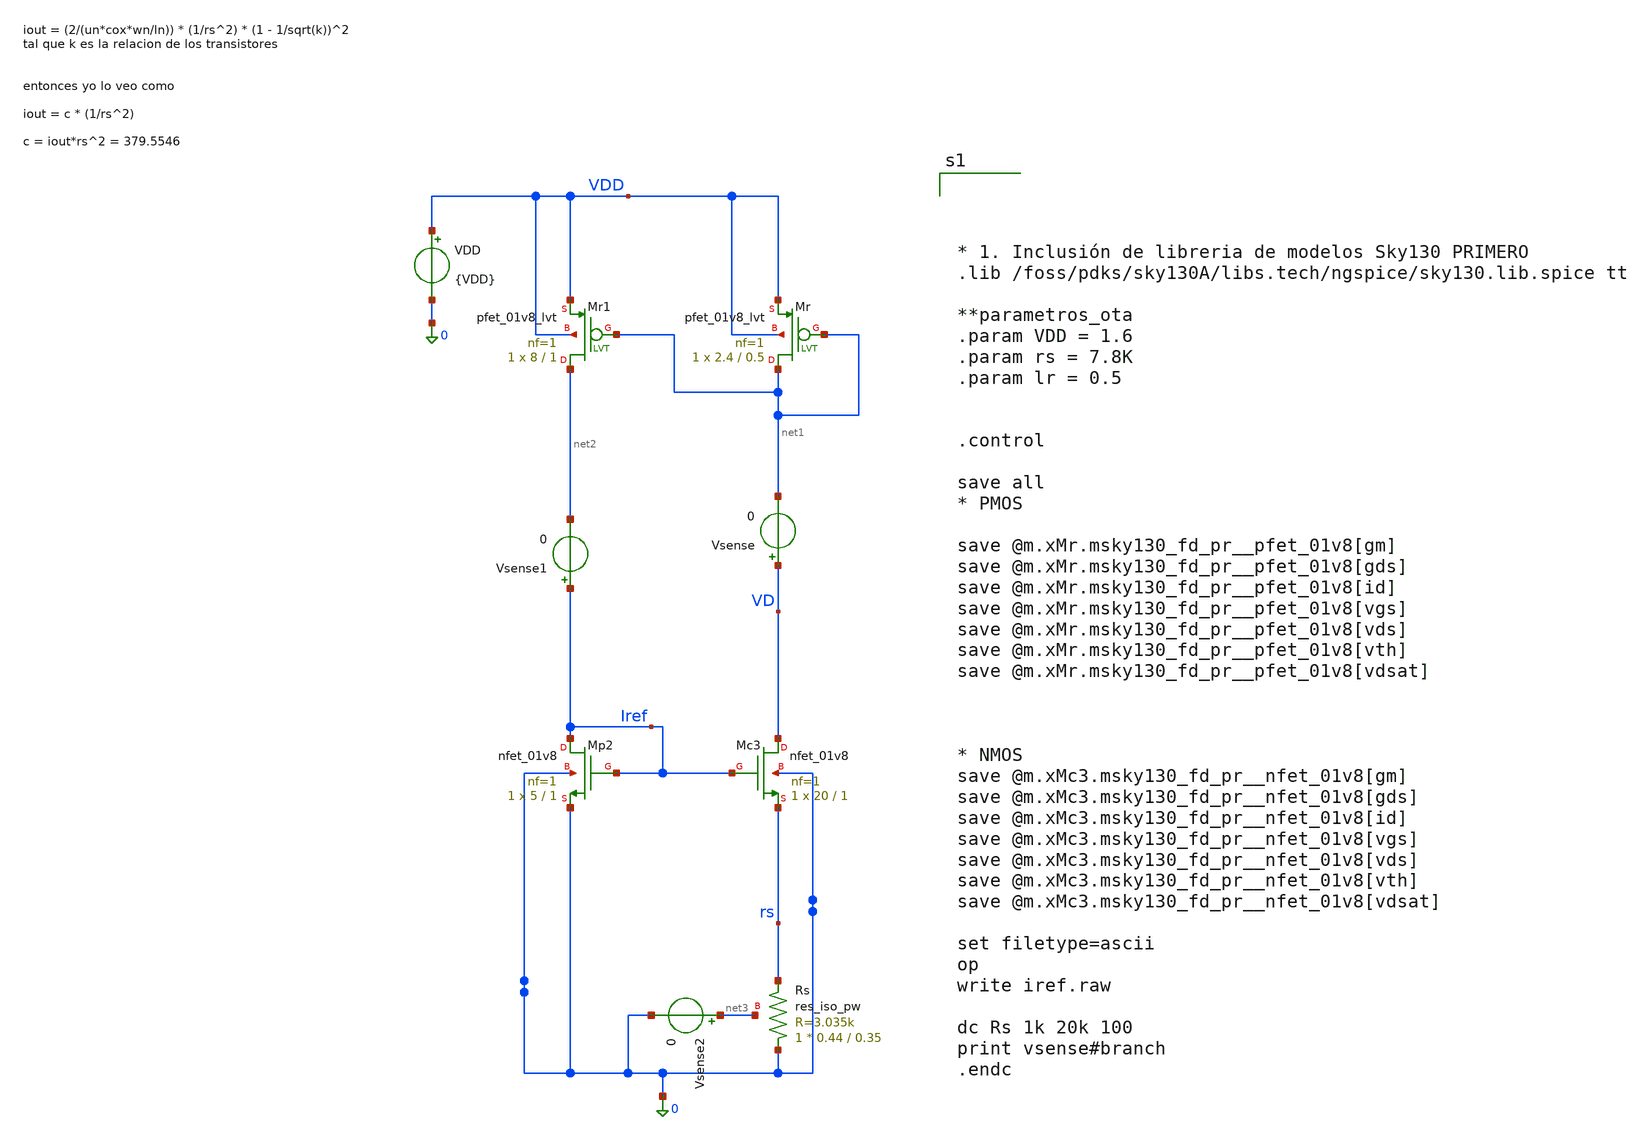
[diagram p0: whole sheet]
** sch_path: xschem/iref.sch
**.subckt iref
XMc3 VD Iref rs 0 sky130_fd_pr__nfet_01v8 L=1 W=20 nf=1 ad='int((1 + 1)/2) * 20 / 1 * 0.29' as='int((1 + 2)/2) * 20 / 1 * 0.29'
+ pd='2*int((1 + 1)/2) * (20 / 1 + 0.29)' ps='2*int((1 + 2)/2) * (20 / 1 + 0.29)' nrd='0.29 / 20 ' nrs='0.29 / 20 '
+ sa=0 sb=0 sd=0 mult=1 m=1
XMp2 Iref Iref 0 0 sky130_fd_pr__nfet_01v8 L=1 W=5 nf=1 ad='int((1 + 1)/2) * 5 / 1 * 0.29' as='int((1 + 2)/2) * 5 / 1 * 0.29'
+ pd='2*int((1 + 1)/2) * (5 / 1 + 0.29)' ps='2*int((1 + 2)/2) * (5 / 1 + 0.29)' nrd='0.29 / 5 ' nrs='0.29 / 5 '
+ sa=0 sb=0 sd=0 mult=1 m=1
XMr net1 net1 VDD VDD sky130_fd_pr__pfet_01v8_lvt L=0.5 W=2.4 nf=1 ad='int((1 + 1)/2) * 2.4 / 1 * 0.29'
+ as='int((1 + 2)/2) * 2.4 / 1 * 0.29' pd='2*int((1 + 1)/2) * (2.4 / 1 + 0.29)' ps='2*int((1 + 2)/2) * (2.4 / 1 + 0.29)'
+ nrd='0.29 / 2.4 ' nrs='0.29 / 2.4 ' sa=0 sb=0 sd=0 mult=1 m=1
XMr1 net2 net1 VDD VDD sky130_fd_pr__pfet_01v8_lvt L=1 W=8 nf=1 ad='int((1 + 1)/2) * 8 / 1 * 0.29' as='int((1 + 2)/2) * 8 / 1 * 0.29'
+ pd='2*int((1 + 1)/2) * (8 / 1 + 0.29)' ps='2*int((1 + 2)/2) * (8 / 1 + 0.29)' nrd='0.29 / 8 ' nrs='0.29 / 8 '
+ sa=0 sb=0 sd=0 mult=1 m=1
Vsense VD net1 0
VDD VDD 0 {VDD}
Vsense1 Iref net2 0
Vsense2 net3 0 0
XRs 0 rs net3 sky130_fd_pr__res_iso_pw W=0.44 L=0.35 m=1
**** begin user architecture code




* 1. Inclusión de libreria de modelos Sky130 PRIMERO
.lib /foss/pdks/sky130A/libs.tech/ngspice/sky130.lib.spice tt

**parametros_ota
.param VDD = 1.6
.param rs = 7.8K
.param lr = 0.5


.control

save all
* PMOS

save @m.xMr.msky130_fd_pr__pfet_01v8[gm]
save @m.xMr.msky130_fd_pr__pfet_01v8[gds]
save @m.xMr.msky130_fd_pr__pfet_01v8[id]
save @m.xMr.msky130_fd_pr__pfet_01v8[vgs]
save @m.xMr.msky130_fd_pr__pfet_01v8[vds]
save @m.xMr.msky130_fd_pr__pfet_01v8[vth]
save @m.xMr.msky130_fd_pr__pfet_01v8[vdsat]



* NMOS
save @m.xMc3.msky130_fd_pr__nfet_01v8[gm]
save @m.xMc3.msky130_fd_pr__nfet_01v8[gds]
save @m.xMc3.msky130_fd_pr__nfet_01v8[id]
save @m.xMc3.msky130_fd_pr__nfet_01v8[vgs]
save @m.xMc3.msky130_fd_pr__nfet_01v8[vds]
save @m.xMc3.msky130_fd_pr__nfet_01v8[vth]
save @m.xMc3.msky130_fd_pr__nfet_01v8[vdsat]

set filetype=ascii
op
write iref.raw

dc Rs 1k 20k 100
print vsense#branch
.endc


**** end user architecture code
**.ends
.end
